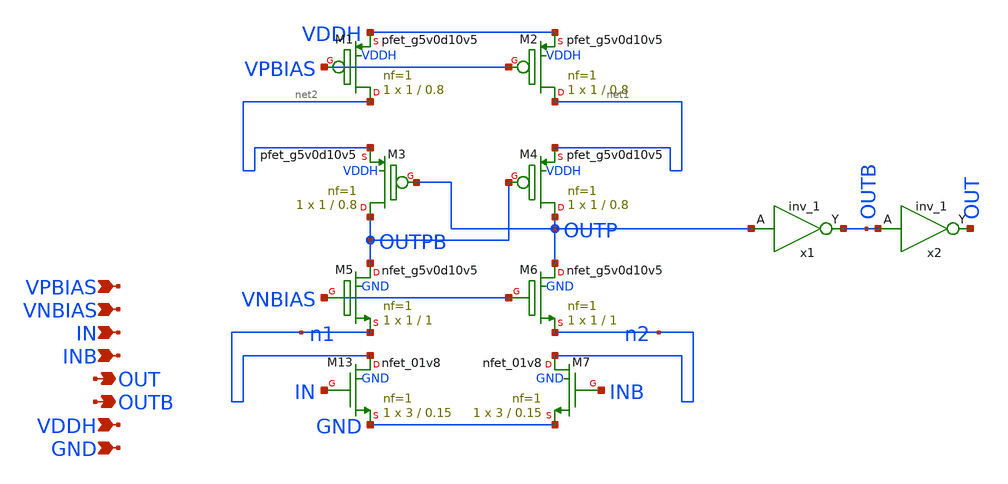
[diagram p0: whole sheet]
** sch_path: xschem/lvsf_1buff.sch
**.subckt lvsf_1buff IN INB OUT VDDH GND VPBIAS VNBIAS OUTB
*.ipin IN
*.ipin INB
*.opin OUT
*.ipin VDDH
*.ipin GND
*.ipin VPBIAS
*.ipin VNBIAS
*.opin OUTB
XM13 n1 IN GND GND sky130_fd_pr__nfet_01v8 L=0.15 W=3 nf=1 ad='int((nf+1)/2) * W/nf * 0.29' as='int((nf+2)/2) * W/nf * 0.29'
+ pd='2*int((nf+1)/2) * (W/nf + 0.29)' ps='2*int((nf+2)/2) * (W/nf + 0.29)' nrd='0.29 / W' nrs='0.29 / W'
+ sa=0 sb=0 sd=0 mult=1 m=1
XM1 net2 VPBIAS VDDH VDDH sky130_fd_pr__pfet_g5v0d10v5 L=0.8 W=1 nf=1 ad='int((nf+1)/2) * W/nf * 0.29'
+ as='int((nf+2)/2) * W/nf * 0.29' pd='2*int((nf+1)/2) * (W/nf + 0.29)' ps='2*int((nf+2)/2) * (W/nf + 0.29)'
+ nrd='0.29 / W' nrs='0.29 / W' sa=0 sb=0 sd=0 mult=1 m=1
XM2 net1 VPBIAS VDDH VDDH sky130_fd_pr__pfet_g5v0d10v5 L=0.8 W=1 nf=1 ad='int((nf+1)/2) * W/nf * 0.29'
+ as='int((nf+2)/2) * W/nf * 0.29' pd='2*int((nf+1)/2) * (W/nf + 0.29)' ps='2*int((nf+2)/2) * (W/nf + 0.29)'
+ nrd='0.29 / W' nrs='0.29 / W' sa=0 sb=0 sd=0 mult=1 m=1
XM3 OUTPB OUTP net2 VDDH sky130_fd_pr__pfet_g5v0d10v5 L=0.8 W=1 nf=1 ad='int((nf+1)/2) * W/nf * 0.29'
+ as='int((nf+2)/2) * W/nf * 0.29' pd='2*int((nf+1)/2) * (W/nf + 0.29)' ps='2*int((nf+2)/2) * (W/nf + 0.29)'
+ nrd='0.29 / W' nrs='0.29 / W' sa=0 sb=0 sd=0 mult=1 m=1
XM4 OUTP OUTPB net1 VDDH sky130_fd_pr__pfet_g5v0d10v5 L=0.8 W=1 nf=1 ad='int((nf+1)/2) * W/nf * 0.29'
+ as='int((nf+2)/2) * W/nf * 0.29' pd='2*int((nf+1)/2) * (W/nf + 0.29)' ps='2*int((nf+2)/2) * (W/nf + 0.29)'
+ nrd='0.29 / W' nrs='0.29 / W' sa=0 sb=0 sd=0 mult=1 m=1
XM5 OUTPB VNBIAS n1 GND sky130_fd_pr__nfet_g5v0d10v5 L=1 W=1 nf=1 ad='int((nf+1)/2) * W/nf * 0.29' as='int((nf+2)/2) * W/nf * 0.29'
+ pd='2*int((nf+1)/2) * (W/nf + 0.29)' ps='2*int((nf+2)/2) * (W/nf + 0.29)' nrd='0.29 / W' nrs='0.29 / W'
+ sa=0 sb=0 sd=0 mult=1 m=1
XM6 OUTP VNBIAS n2 GND sky130_fd_pr__nfet_g5v0d10v5 L=1 W=1 nf=1 ad='int((nf+1)/2) * W/nf * 0.29' as='int((nf+2)/2) * W/nf * 0.29'
+ pd='2*int((nf+1)/2) * (W/nf + 0.29)' ps='2*int((nf+2)/2) * (W/nf + 0.29)' nrd='0.29 / W' nrs='0.29 / W'
+ sa=0 sb=0 sd=0 mult=1 m=1
XM7 n2 INB GND GND sky130_fd_pr__nfet_01v8 L=0.15 W=3 nf=1 ad='int((nf+1)/2) * W/nf * 0.29' as='int((nf+2)/2) * W/nf * 0.29'
+ pd='2*int((nf+1)/2) * (W/nf + 0.29)' ps='2*int((nf+2)/2) * (W/nf + 0.29)' nrd='0.29 / W' nrs='0.29 / W'
+ sa=0 sb=0 sd=0 mult=1 m=1
x1 OUTP GND GND VDDH VDDH OUTB sky130_fd_sc_hvl__inv_1
x2 OUTB GND GND VDDH VDDH OUT sky130_fd_sc_hvl__inv_1
**.ends
.end
